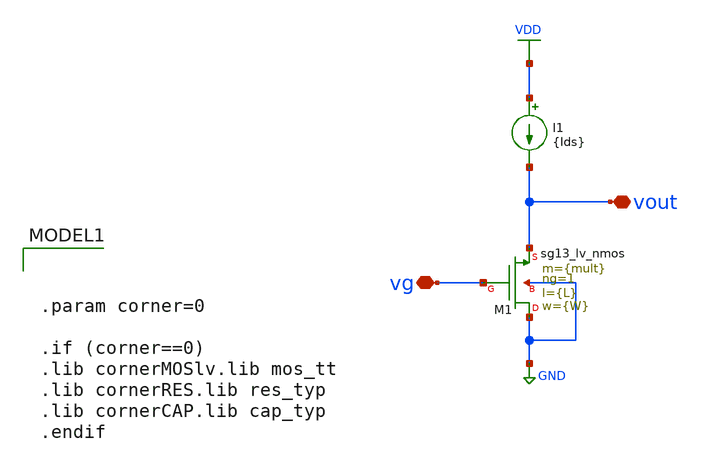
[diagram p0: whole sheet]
** sch_path: Taller2_extendido/Insumos/cs_amp_full_IPD413HW1.sch
**.subckt cs_amp_full_IPD413HW1 vg vout
*.iopin vg
*.iopin vout
I1 VDD vout {Ids}
XM1 GND vg vout GND sg13_lv_nmos w={W} l={L} ng=1 m={mult} mm_ok=1
**** begin user architecture code


.param corner=0

.if (corner==0)
.lib cornerMOSlv.lib mos_tt
.lib cornerRES.lib res_typ
.lib cornerCAP.lib cap_typ
.endif



.option wnflag=1
.param gm    = {3.1415*1.1m}
.param gm_id = 13
.param Ids   = {gm/gm_id}
.param L     = 0.13u
.param W     = 3.13u
.param mult  = 10

vsup VDD 0 1.2
vin vg 0 dc=0.45 ac=1

cload vout 0 5p

.control
save all
op
save @n.xm1.nsg13_lv_nmos[gm]
save @n.xm1.nsg13_lv_nmos[ids]
save @n.xm1.nsg13_lv_nmos[gds]
save @n.xm1.nsg13_lv_nmos[ib]

*dc vin -0.01 0.01 0.001
dc vin 0.45 0.45 0.001
***********************************************
* Ingresar comando de ganancias acá



* *********************************************

***********************************************
* Ingresar comando de simulación AC y mediciones acá



* *********************************************
.endc

**** end user architecture code
**.ends
.GLOBAL GND
.GLOBAL VDD
.end
